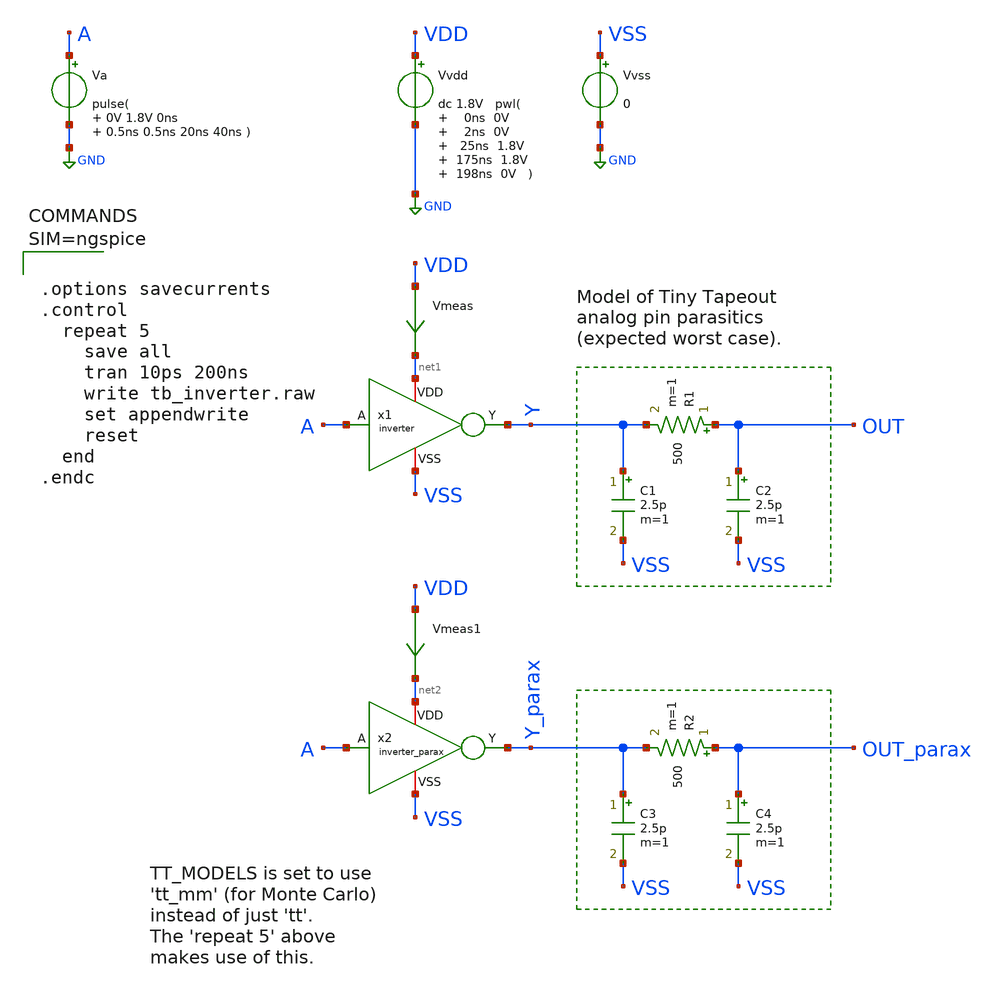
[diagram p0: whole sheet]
** sch_path: xschem/tb_inverter.sch
**.subckt tb_inverter
x1 net1 VSS A Y inverter
Vvss VSS GND 0
Vvdd VDD GND dc 1.8V pwl( 0ns 0V 2ns 0V 25ns 1.8V 175ns 1.8V 198ns 0V )
Va A GND pulse( 0V 1.8V 0ns 0.5ns 0.5ns 20ns 40ns )
R1 OUT Y 500 m=1
C1 Y VSS 2.5p m=1
C2 OUT VSS 2.5p m=1
Vmeas VDD net1 0
.save i(vmeas)
x2 net2 VSS A Y_parax inverter_parax
R2 OUT_parax Y_parax 500 m=1
C3 Y_parax VSS 2.5p m=1
C4 OUT_parax VSS 2.5p m=1
Vmeas1 VDD net2 0
.save i(vmeas1)
**** begin user architecture code

** opencircuitdesign pdks install
.lib $::SKYWATER_MODELS/sky130.lib.spice tt_mm





.options savecurrents
.control
  repeat 5
    save all
    tran 10ps 200ns
    write tb_inverter.raw
    set appendwrite
    reset
  end
.endc



**** end user architecture code
**.ends

* expanding   symbol:  inverter.sym # of pins=4
** sym_path: xschem/inverter.sym
** sch_path: xschem/inverter.sch
.subckt inverter VDD VSS A Y
*.iopin VDD
*.iopin VSS
*.ipin A
*.opin Y
XM1 Y A VDD VDD sky130_fd_pr__pfet_01v8 L=0.15 W=2 nf=1 ad='int((nf+1)/2) * W/nf * 0.29' as='int((nf+2)/2) * W/nf * 0.29'
+ pd='2*int((nf+1)/2) * (W/nf + 0.29)' ps='2*int((nf+2)/2) * (W/nf + 0.29)' nrd='0.29 / W' nrs='0.29 / W'
+ sa=0 sb=0 sd=0 mult=1 m=1
XM2 Y A VSS VSS sky130_fd_pr__nfet_01v8 L=0.15 W=1 nf=1 ad='int((nf+1)/2) * W/nf * 0.29' as='int((nf+2)/2) * W/nf * 0.29'
+ pd='2*int((nf+1)/2) * (W/nf + 0.29)' ps='2*int((nf+2)/2) * (W/nf + 0.29)' nrd='0.29 / W' nrs='0.29 / W'
+ sa=0 sb=0 sd=0 mult=1 m=1
.ends


* expanding   symbol:  inverter_parax.sym # of pins=4
** sym_path: xschem/inverter.sym
.include [file normalize ../mag/inverter.sim.spice]
.GLOBAL GND
.end
